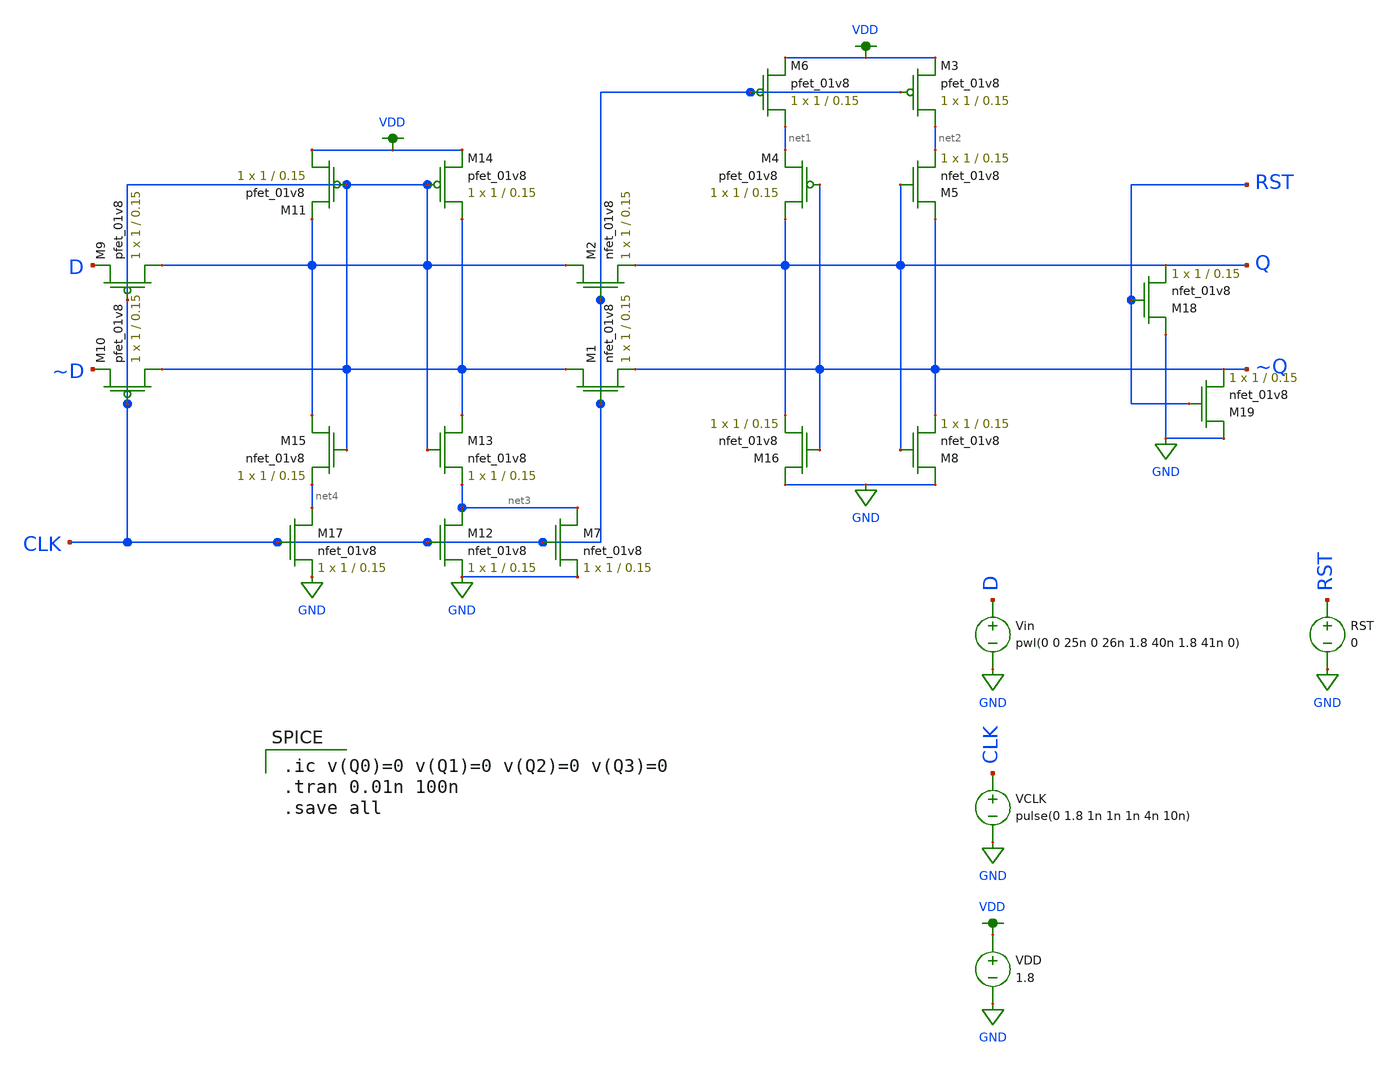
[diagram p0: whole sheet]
** sch_path: shift register/full_shift_register.sch
**.subckt full_shift_register
XM17 net4 CLK GND GND sky130_fd_pr__nfet_01v8 L=0.15 W=1 nf=1 ad='int((nf+1)/2) * W/nf * 0.29' as='int((nf+2)/2) * W/nf * 0.29'
+ pd='2*int((nf+1)/2) * (W/nf + 0.29)' ps='2*int((nf+2)/2) * (W/nf + 0.29)' nrd='0.29 / W' nrs='0.29 / W'
+ sa=0 sb=0 sd=0 mult=1 m=1
XM12 net3 CLK GND GND sky130_fd_pr__nfet_01v8 L=0.15 W=1 nf=1 ad='int((nf+1)/2) * W/nf * 0.29' as='int((nf+2)/2) * W/nf * 0.29'
+ pd='2*int((nf+1)/2) * (W/nf + 0.29)' ps='2*int((nf+2)/2) * (W/nf + 0.29)' nrd='0.29 / W' nrs='0.29 / W'
+ sa=0 sb=0 sd=0 mult=1 m=1
XM13 CLK CLK net3 GND sky130_fd_pr__nfet_01v8 L=0.15 W=1 nf=1 ad='int((nf+1)/2) * W/nf * 0.29' as='int((nf+2)/2) * W/nf * 0.29'
+ pd='2*int((nf+1)/2) * (W/nf + 0.29)' ps='2*int((nf+2)/2) * (W/nf + 0.29)' nrd='0.29 / W' nrs='0.29 / W'
+ sa=0 sb=0 sd=0 mult=1 m=1
XM15 CLK CLK net4 GND sky130_fd_pr__nfet_01v8 L=0.15 W=1 nf=1 ad='int((nf+1)/2) * W/nf * 0.29' as='int((nf+2)/2) * W/nf * 0.29'
+ pd='2*int((nf+1)/2) * (W/nf + 0.29)' ps='2*int((nf+2)/2) * (W/nf + 0.29)' nrd='0.29 / W' nrs='0.29 / W'
+ sa=0 sb=0 sd=0 mult=1 m=1
XM1 CLK CLK ~Q GND sky130_fd_pr__nfet_01v8 L=0.15 W=1 nf=1 ad='int((nf+1)/2) * W/nf * 0.29' as='int((nf+2)/2) * W/nf * 0.29'
+ pd='2*int((nf+1)/2) * (W/nf + 0.29)' ps='2*int((nf+2)/2) * (W/nf + 0.29)' nrd='0.29 / W' nrs='0.29 / W'
+ sa=0 sb=0 sd=0 mult=1 m=1
XM2 CLK CLK Q GND sky130_fd_pr__nfet_01v8 L=0.15 W=1 nf=1 ad='int((nf+1)/2) * W/nf * 0.29' as='int((nf+2)/2) * W/nf * 0.29'
+ pd='2*int((nf+1)/2) * (W/nf + 0.29)' ps='2*int((nf+2)/2) * (W/nf + 0.29)' nrd='0.29 / W' nrs='0.29 / W'
+ sa=0 sb=0 sd=0 mult=1 m=1
XM8 GND Q ~Q GND sky130_fd_pr__nfet_01v8 L=0.15 W=1 nf=1 ad='int((nf+1)/2) * W/nf * 0.29' as='int((nf+2)/2) * W/nf * 0.29'
+ pd='2*int((nf+1)/2) * (W/nf + 0.29)' ps='2*int((nf+2)/2) * (W/nf + 0.29)' nrd='0.29 / W' nrs='0.29 / W'
+ sa=0 sb=0 sd=0 mult=1 m=1
XM4 Q ~Q net1 VDD sky130_fd_pr__pfet_01v8 L=0.15 W=1 nf=1 ad='int((nf+1)/2) * W/nf * 0.29' as='int((nf+2)/2) * W/nf * 0.29'
+ pd='2*int((nf+1)/2) * (W/nf + 0.29)' ps='2*int((nf+2)/2) * (W/nf + 0.29)' nrd='0.29 / W' nrs='0.29 / W'
+ sa=0 sb=0 sd=0 mult=1 m=1
XM3 net2 CLK VDD VDD sky130_fd_pr__pfet_01v8 L=0.15 W=1 nf=1 ad='int((nf+1)/2) * W/nf * 0.29' as='int((nf+2)/2) * W/nf * 0.29'
+ pd='2*int((nf+1)/2) * (W/nf + 0.29)' ps='2*int((nf+2)/2) * (W/nf + 0.29)' nrd='0.29 / W' nrs='0.29 / W'
+ sa=0 sb=0 sd=0 mult=1 m=1
XM6 net1 CLK VDD VDD sky130_fd_pr__pfet_01v8 L=0.15 W=1 nf=1 ad='int((nf+1)/2) * W/nf * 0.29' as='int((nf+2)/2) * W/nf * 0.29'
+ pd='2*int((nf+1)/2) * (W/nf + 0.29)' ps='2*int((nf+2)/2) * (W/nf + 0.29)' nrd='0.29 / W' nrs='0.29 / W'
+ sa=0 sb=0 sd=0 mult=1 m=1
XM10 CLK CLK ~D VDD sky130_fd_pr__pfet_01v8 L=0.15 W=1 nf=1 ad='int((nf+1)/2) * W/nf * 0.29' as='int((nf+2)/2) * W/nf * 0.29'
+ pd='2*int((nf+1)/2) * (W/nf + 0.29)' ps='2*int((nf+2)/2) * (W/nf + 0.29)' nrd='0.29 / W' nrs='0.29 / W'
+ sa=0 sb=0 sd=0 mult=1 m=1
XM9 CLK CLK D VDD sky130_fd_pr__pfet_01v8 L=0.15 W=1 nf=1 ad='int((nf+1)/2) * W/nf * 0.29' as='int((nf+2)/2) * W/nf * 0.29'
+ pd='2*int((nf+1)/2) * (W/nf + 0.29)' ps='2*int((nf+2)/2) * (W/nf + 0.29)' nrd='0.29 / W' nrs='0.29 / W'
+ sa=0 sb=0 sd=0 mult=1 m=1
XM11 VDD CLK CLK VDD sky130_fd_pr__pfet_01v8 L=0.15 W=1 nf=1 ad='int((nf+1)/2) * W/nf * 0.29' as='int((nf+2)/2) * W/nf * 0.29'
+ pd='2*int((nf+1)/2) * (W/nf + 0.29)' ps='2*int((nf+2)/2) * (W/nf + 0.29)' nrd='0.29 / W' nrs='0.29 / W'
+ sa=0 sb=0 sd=0 mult=1 m=1
XM14 CLK CLK VDD VDD sky130_fd_pr__pfet_01v8 L=0.15 W=1 nf=1 ad='int((nf+1)/2) * W/nf * 0.29' as='int((nf+2)/2) * W/nf * 0.29'
+ pd='2*int((nf+1)/2) * (W/nf + 0.29)' ps='2*int((nf+2)/2) * (W/nf + 0.29)' nrd='0.29 / W' nrs='0.29 / W'
+ sa=0 sb=0 sd=0 mult=1 m=1
XM16 GND ~Q Q GND sky130_fd_pr__nfet_01v8 L=0.15 W=1 nf=1 ad='int((nf+1)/2) * W/nf * 0.29' as='int((nf+2)/2) * W/nf * 0.29'
+ pd='2*int((nf+1)/2) * (W/nf + 0.29)' ps='2*int((nf+2)/2) * (W/nf + 0.29)' nrd='0.29 / W' nrs='0.29 / W'
+ sa=0 sb=0 sd=0 mult=1 m=1
XM5 ~Q Q net2 GND sky130_fd_pr__nfet_01v8 L=0.15 W=1 nf=1 ad='int((nf+1)/2) * W/nf * 0.29' as='int((nf+2)/2) * W/nf * 0.29'
+ pd='2*int((nf+1)/2) * (W/nf + 0.29)' ps='2*int((nf+2)/2) * (W/nf + 0.29)' nrd='0.29 / W' nrs='0.29 / W'
+ sa=0 sb=0 sd=0 mult=1 m=1
XM7 net3 CLK GND GND sky130_fd_pr__nfet_01v8 L=0.15 W=1 nf=1 ad='int((nf+1)/2) * W/nf * 0.29' as='int((nf+2)/2) * W/nf * 0.29'
+ pd='2*int((nf+1)/2) * (W/nf + 0.29)' ps='2*int((nf+2)/2) * (W/nf + 0.29)' nrd='0.29 / W' nrs='0.29 / W'
+ sa=0 sb=0 sd=0 mult=1 m=1
XM18 GND RST Q GND sky130_fd_pr__nfet_01v8 L=0.15 W=1 nf=1 ad='int((nf+1)/2) * W/nf * 0.29' as='int((nf+2)/2) * W/nf * 0.29'
+ pd='2*int((nf+1)/2) * (W/nf + 0.29)' ps='2*int((nf+2)/2) * (W/nf + 0.29)' nrd='0.29 / W' nrs='0.29 / W'
+ sa=0 sb=0 sd=0 mult=1 m=1
XM19 GND RST ~Q GND sky130_fd_pr__nfet_01v8 L=0.15 W=1 nf=1 ad='int((nf+1)/2) * W/nf * 0.29' as='int((nf+2)/2) * W/nf * 0.29'
+ pd='2*int((nf+1)/2) * (W/nf + 0.29)' ps='2*int((nf+2)/2) * (W/nf + 0.29)' nrd='0.29 / W' nrs='0.29 / W'
+ sa=0 sb=0 sd=0 mult=1 m=1
VDD VDD GND 1.8
VCLK CLK GND pulse(0 1.8 1n 1n 1n 4n 10n)
Vin D GND pwl(0 0 25n 0 26n 1.8 40n 1.8 41n 0)
RST RST GND 0
**** begin user architecture code

.ic v(Q0)=0 v(Q1)=0 v(Q2)=0 v(Q3)=0
.tran 0.01n 100n
.save all


.option wnflag=1
.lib ~/home/ttuser/Documents/image_processing_final/madvlsi/sf_models.sym

**** end user architecture code
**.ends
.GLOBAL GND
.GLOBAL VDD
.end
